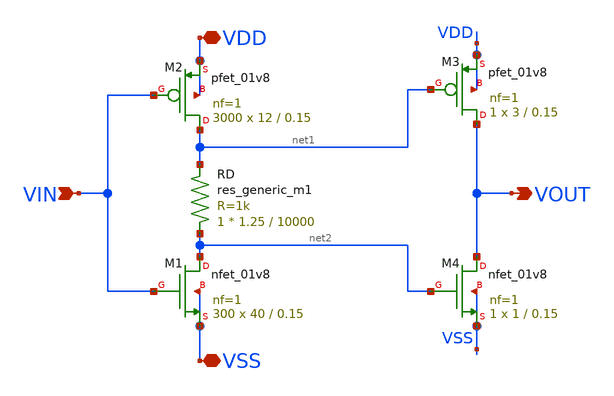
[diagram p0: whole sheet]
** sch_path: xschem/DC_DC_Converter_xschem/OTHERS/DC_DC_Converter0/Inverter_4/Inverter4.sch
**.subckt Inverter4 VIN VDD VSS VOUT
*.ipin VIN
*.iopin VDD
*.iopin VSS
*.opin VOUT
XM1 net2 VIN VSS VSS sky130_fd_pr__nfet_01v8 L=0.15 W=40 nf=1 ad='int((nf+1)/2) * W/nf * 0.29' as='int((nf+2)/2) * W/nf * 0.29'
+ pd='2*int((nf+1)/2) * (W/nf + 0.29)' ps='2*int((nf+2)/2) * (W/nf + 0.29)' nrd='0.29 / W' nrs='0.29 / W'
+ sa=0 sb=0 sd=0 mult=300 m=300
XM2 net1 VIN VDD VDD sky130_fd_pr__pfet_01v8 L=0.15 W=12 nf=1 ad='int((nf+1)/2) * W/nf * 0.29' as='int((nf+2)/2) * W/nf * 0.29'
+ pd='2*int((nf+1)/2) * (W/nf + 0.29)' ps='2*int((nf+2)/2) * (W/nf + 0.29)' nrd='0.29 / W' nrs='0.29 / W'
+ sa=0 sb=0 sd=0 mult=3000 m=3000
RD net2 net1 sky130_fd_pr__res_generic_m1 W=1.25 L=10000 m=1
XM3 VOUT net1 VDD VDD sky130_fd_pr__pfet_01v8 L=0.15 W=3 nf=1 ad='int((nf+1)/2) * W/nf * 0.29' as='int((nf+2)/2) * W/nf * 0.29'
+ pd='2*int((nf+1)/2) * (W/nf + 0.29)' ps='2*int((nf+2)/2) * (W/nf + 0.29)' nrd='0.29 / W' nrs='0.29 / W'
+ sa=0 sb=0 sd=0 mult=1 m=1
XM4 VOUT net2 VSS VSS sky130_fd_pr__nfet_01v8 L=0.15 W=1 nf=1 ad='int((nf+1)/2) * W/nf * 0.29' as='int((nf+2)/2) * W/nf * 0.29'
+ pd='2*int((nf+1)/2) * (W/nf + 0.29)' ps='2*int((nf+2)/2) * (W/nf + 0.29)' nrd='0.29 / W' nrs='0.29 / W'
+ sa=0 sb=0 sd=0 mult=1 m=1
**.ends
.end
